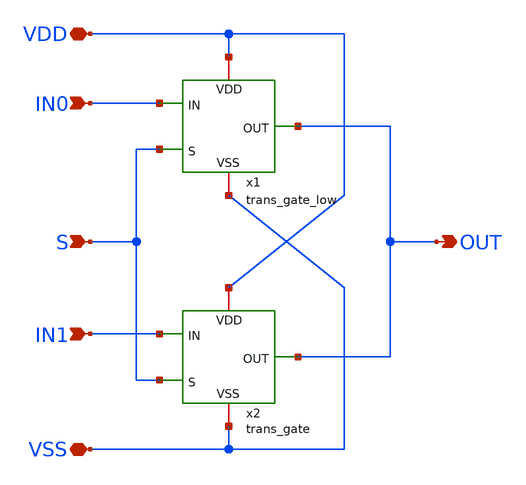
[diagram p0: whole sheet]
** sch_path: SSDOR_1.2V_v2/components/mux2/mux2.sch
**.subckt mux2 IN0 S IN1 VDD VSS OUT
*.ipin IN0
*.ipin S
*.ipin IN1
*.iopin VDD
*.iopin VSS
*.opin OUT
x2 OUT IN1 VDD S VSS trans_gate
x1 OUT IN0 VDD S VSS trans_gate_low
**.ends
.end
